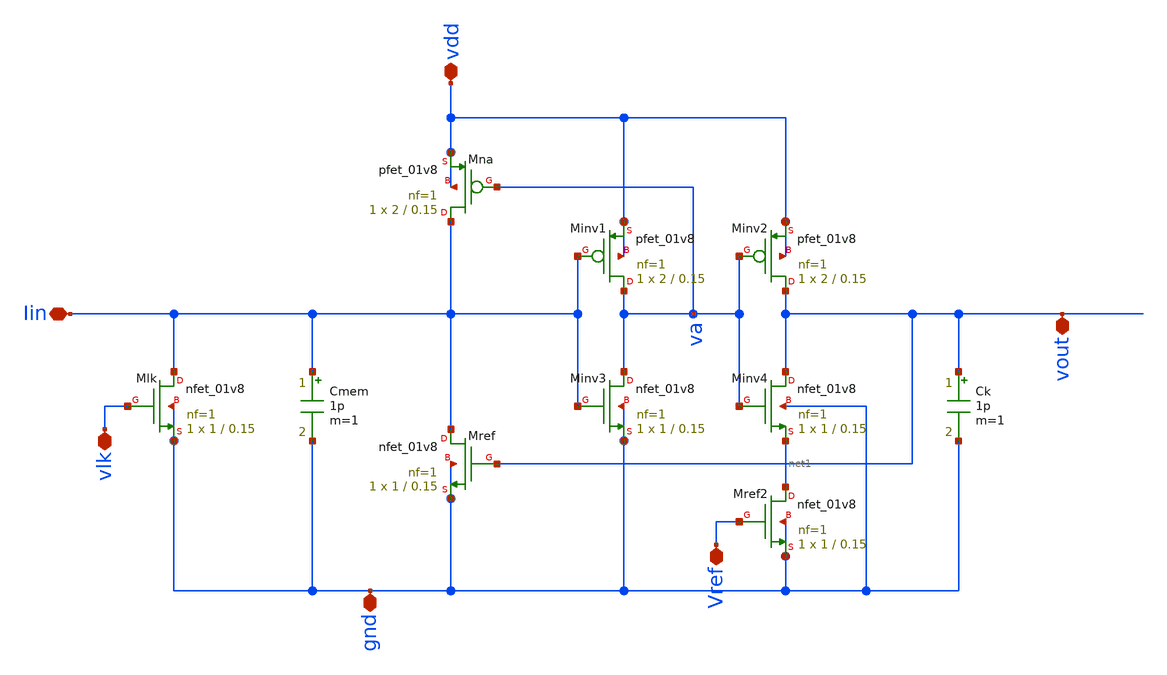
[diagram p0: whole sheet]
** sch_path: Neuron/OZNeuron/ozneuron.sch
**.subckt ozneuron Vref gnd vdd vlk vout Iin
*.iopin Vref
*.iopin gnd
*.iopin vdd
*.iopin vlk
*.iopin vout
*.iopin Iin
XMna Iin va vdd vdd sky130_fd_pr__pfet_01v8 L=0.15 W=2 nf=1 ad='int((nf+1)/2) * W/nf * 0.29' as='int((nf+2)/2) * W/nf * 0.29'
+ pd='2*int((nf+1)/2) * (W/nf + 0.29)' ps='2*int((nf+2)/2) * (W/nf + 0.29)' nrd='0.29 / W' nrs='0.29 / W'
+ sa=0 sb=0 sd=0 mult=1 m=1
XMlk Iin vlk gnd gnd sky130_fd_pr__nfet_01v8 L=0.15 W=1 nf=1 ad='int((1 + 1)/2) * 1 / 1 * 0.29' as='int((1 + 2)/2) * 1 / 1 * 0.29'
+ pd='2*int((1 + 1)/2) * (1 / 1 + 0.29)' ps='2*int((1 + 2)/2) * (1 / 1 + 0.29)' nrd='0.29 / 1 ' nrs='0.29 / 1 '
+ sa=0 sb=0 sd=0 mult=1 m=1
XMinv1 va Iin vdd vdd sky130_fd_pr__pfet_01v8 L=0.15 W=2 nf=1 ad='int((nf+1)/2) * W/nf * 0.29' as='int((nf+2)/2) * W/nf * 0.29'
+ pd='2*int((nf+1)/2) * (W/nf + 0.29)' ps='2*int((nf+2)/2) * (W/nf + 0.29)' nrd='0.29 / W' nrs='0.29 / W'
+ sa=0 sb=0 sd=0 mult=1 m=1
XMinv2 vout va vdd vdd sky130_fd_pr__pfet_01v8 L=0.15 W=2 nf=1 ad='int((nf+1)/2) * W/nf * 0.29' as='int((nf+2)/2) * W/nf * 0.29'
+ pd='2*int((nf+1)/2) * (W/nf + 0.29)' ps='2*int((nf+2)/2) * (W/nf + 0.29)' nrd='0.29 / W' nrs='0.29 / W'
+ sa=0 sb=0 sd=0 mult=1 m=1
XMref Iin vout gnd gnd sky130_fd_pr__nfet_01v8 L=0.15 W=1 nf=1 ad='int((1 + 1)/2) * 1 / 1 * 0.29' as='int((1 + 2)/2) * 1 / 1 * 0.29'
+ pd='2*int((1 + 1)/2) * (1 / 1 + 0.29)' ps='2*int((1 + 2)/2) * (1 / 1 + 0.29)' nrd='0.29 / 1 ' nrs='0.29 / 1 '
+ sa=0 sb=0 sd=0 mult=1 m=1
XMinv3 va Iin gnd gnd sky130_fd_pr__nfet_01v8 L=0.15 W=1 nf=1 ad='int((1 + 1)/2) * 1 / 1 * 0.29' as='int((1 + 2)/2) * 1 / 1 * 0.29'
+ pd='2*int((1 + 1)/2) * (1 / 1 + 0.29)' ps='2*int((1 + 2)/2) * (1 / 1 + 0.29)' nrd='0.29 / 1 ' nrs='0.29 / 1 '
+ sa=0 sb=0 sd=0 mult=1 m=1
XMinv4 vout va net1 gnd sky130_fd_pr__nfet_01v8 L=0.15 W=1 nf=1 ad='int((1 + 1)/2) * 1 / 1 * 0.29' as='int((1 + 2)/2) * 1 / 1 * 0.29'
+ pd='2*int((1 + 1)/2) * (1 / 1 + 0.29)' ps='2*int((1 + 2)/2) * (1 / 1 + 0.29)' nrd='0.29 / 1 ' nrs='0.29 / 1 '
+ sa=0 sb=0 sd=0 mult=1 m=1
XMref2 net1 Vref gnd gnd sky130_fd_pr__nfet_01v8 L=0.15 W=1 nf=1 ad='int((1 + 1)/2) * 1 / 1 * 0.29' as='int((1 + 2)/2) * 1 / 1 * 0.29'
+ pd='2*int((1 + 1)/2) * (1 / 1 + 0.29)' ps='2*int((1 + 2)/2) * (1 / 1 + 0.29)' nrd='0.29 / 1 ' nrs='0.29 / 1 '
+ sa=0 sb=0 sd=0 mult=1 m=1
Cmem Iin gnd 1p m=1
Ck vout gnd 1p m=1
**.ends
.end
